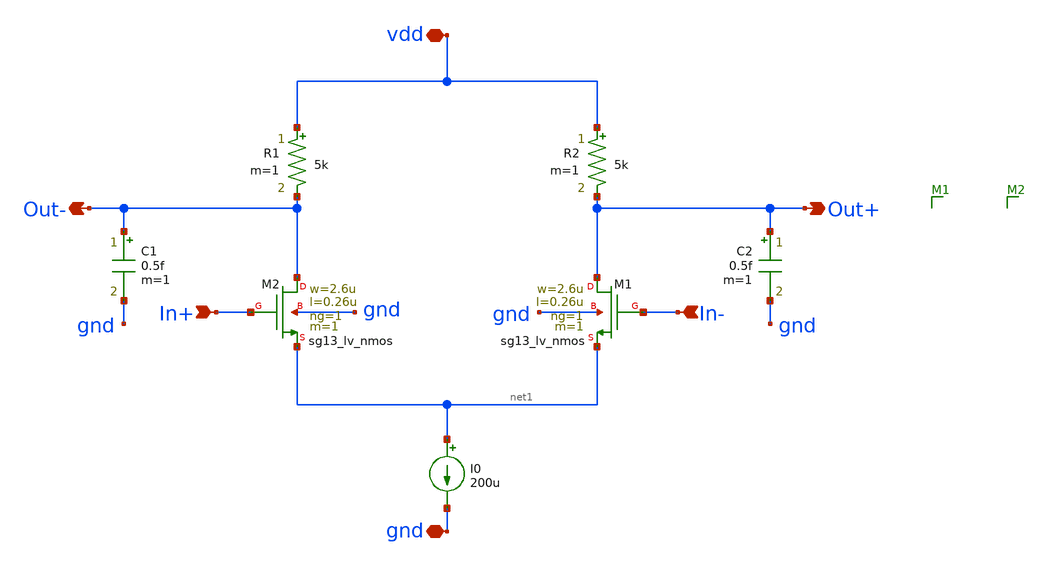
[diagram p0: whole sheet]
** sch_path: modules/module_4_type_2_PLL/diff_Roscillator/schematic/differential_core.sch
**.subckt differential_core In+ vdd gnd In- Out+ Out-
*.ipin In+
*.iopin vdd
*.iopin gnd
*.ipin In-
*.opin Out+
*.opin Out-
XM1 Out+ In- net1 gnd sg13_lv_nmos w=2.6u l=0.26u ng=1 m=1 mm_ok=1
XM2 Out- In+ net1 gnd sg13_lv_nmos w=2.6u l=0.26u ng=1 m=1 mm_ok=1
R1 vdd Out- 5k m=1
R2 vdd Out+ 5k m=1
C1 Out- gnd 0.5f m=1
C2 Out+ gnd 0.5f m=1
I0 net1 gnd 200u
**.ends
.end
